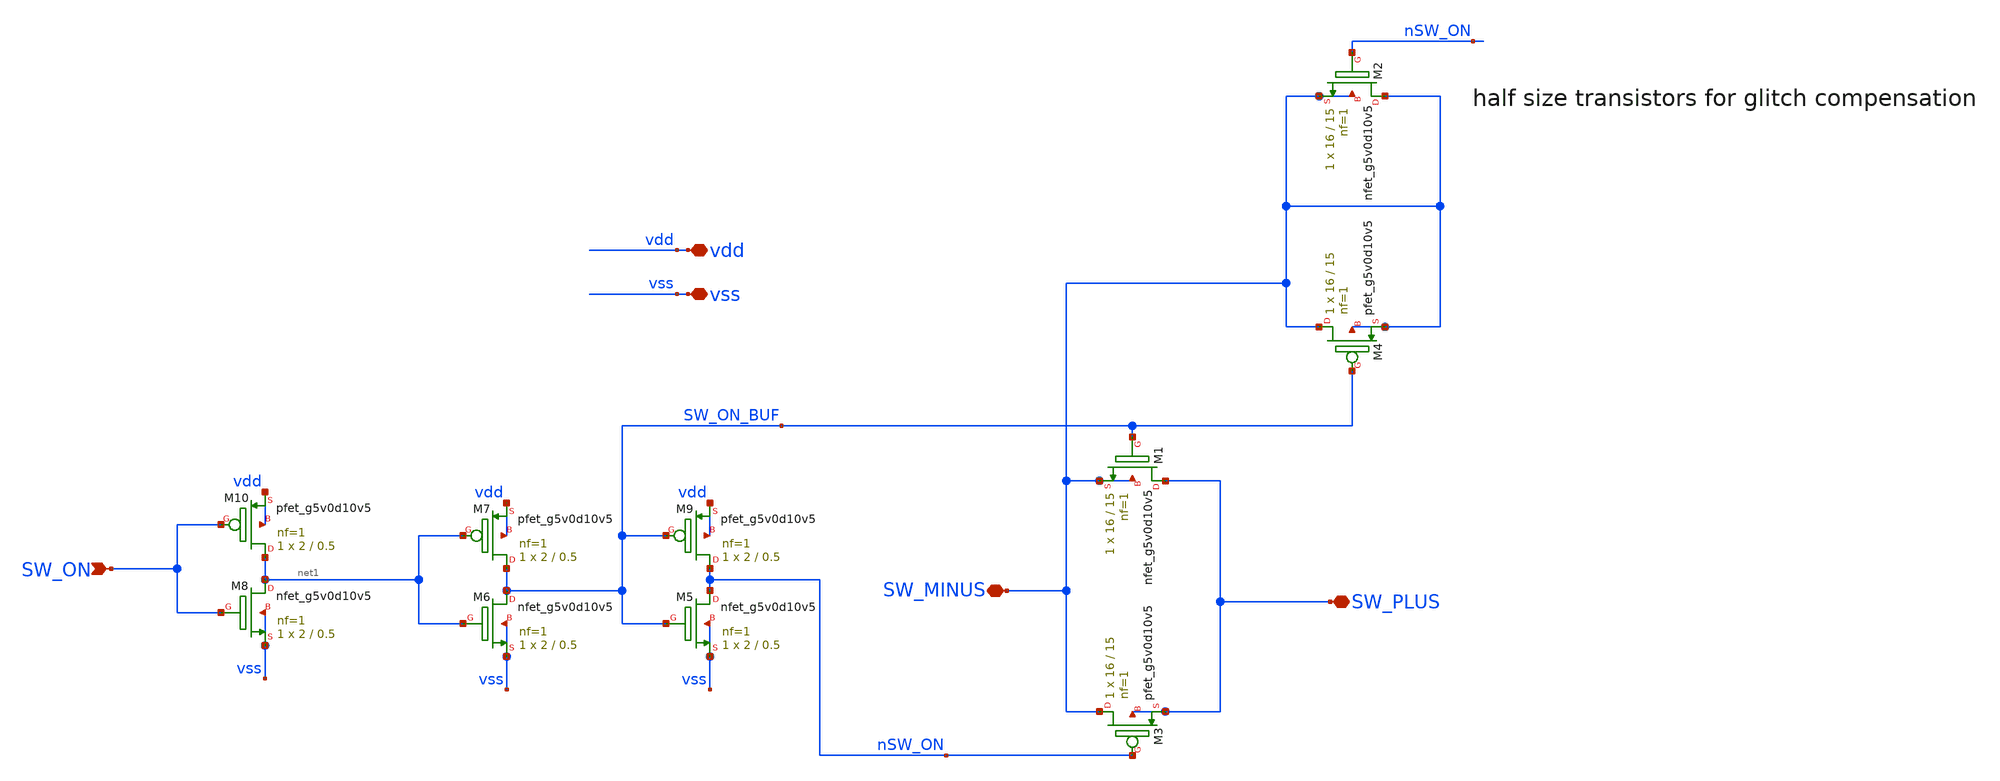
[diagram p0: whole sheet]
** sch_path: xschem/analog_switch.sch
**.subckt analog_switch vdd vss SW_ON SW_MINUS SW_PLUS
*.iopin vdd
*.iopin vss
*.ipin SW_ON
*.iopin SW_MINUS
*.iopin SW_PLUS
XM1 SW_PLUS SW_ON_BUF SW_MINUS SW_MINUS sky130_fd_pr__nfet_g5v0d10v5 L=15 W=16 nf=1 ad='int((1 + 1)/2) * 16 / 1 * 0.29'
+ as='int((1 + 2)/2) * 16 / 1 * 0.29' pd='2*int((1 + 1)/2) * (16 / 1 + 0.29)' ps='2*int((1 + 2)/2) * (16 / 1 + 0.29)'
+ nrd='0.29 / 16 ' nrs='0.29 / 16 ' sa=0 sb=0 sd=0 mult=1 m=1
XM3 SW_MINUS nSW_ON SW_PLUS SW_PLUS sky130_fd_pr__pfet_g5v0d10v5 L=15 W=16 nf=1 ad='int((1 + 1)/2) * 16 / 1 * 0.29'
+ as='int((1 + 2)/2) * 16 / 1 * 0.29' pd='2*int((1 + 1)/2) * (16 / 1 + 0.29)' ps='2*int((1 + 2)/2) * (16 / 1 + 0.29)'
+ nrd='0.29 / 16 ' nrs='0.29 / 16 ' sa=0 sb=0 sd=0 mult=1 m=1
XM2 SW_MINUS nSW_ON SW_MINUS SW_MINUS sky130_fd_pr__nfet_g5v0d10v5 L=15 W=16 nf=1 ad='int((1 + 1)/2) * 16 / 1 * 0.29'
+ as='int((1 + 2)/2) * 16 / 1 * 0.29' pd='2*int((1 + 1)/2) * (16 / 1 + 0.29)' ps='2*int((1 + 2)/2) * (16 / 1 + 0.29)'
+ nrd='0.29 / 16 ' nrs='0.29 / 16 ' sa=0 sb=0 sd=0 mult=1 m=1
XM4 SW_MINUS SW_ON_BUF SW_MINUS SW_MINUS sky130_fd_pr__pfet_g5v0d10v5 L=15 W=16 nf=1 ad='int((1 + 1)/2) * 16 / 1 * 0.29'
+ as='int((1 + 2)/2) * 16 / 1 * 0.29' pd='2*int((1 + 1)/2) * (16 / 1 + 0.29)' ps='2*int((1 + 2)/2) * (16 / 1 + 0.29)'
+ nrd='0.29 / 16 ' nrs='0.29 / 16 ' sa=0 sb=0 sd=0 mult=1 m=1
XM6 SW_ON_BUF net1 vss vss sky130_fd_pr__nfet_g5v0d10v5 L=0.5 W=2 nf=1 ad='int((1 + 1)/2) * 2 / 1 * 0.29'
+ as='int((1 + 2)/2) * 2 / 1 * 0.29' pd='2*int((1 + 1)/2) * (2 / 1 + 0.29)' ps='2*int((1 + 2)/2) * (2 / 1 + 0.29)'
+ nrd='0.29 / 2 ' nrs='0.29 / 2 ' sa=0 sb=0 sd=0 mult=1 m=1
XM7 SW_ON_BUF net1 vdd vdd sky130_fd_pr__pfet_g5v0d10v5 L=0.5 W=2 nf=1 ad='int((1 + 1)/2) * 2 / 1 * 0.29'
+ as='int((1 + 2)/2) * 2 / 1 * 0.29' pd='2*int((1 + 1)/2) * (2 / 1 + 0.29)' ps='2*int((1 + 2)/2) * (2 / 1 + 0.29)'
+ nrd='0.29 / 2 ' nrs='0.29 / 2 ' sa=0 sb=0 sd=0 mult=1 m=1
XM8 net1 SW_ON vss vss sky130_fd_pr__nfet_g5v0d10v5 L=0.5 W=2 nf=1 ad='int((1 + 1)/2) * 2 / 1 * 0.29'
+ as='int((1 + 2)/2) * 2 / 1 * 0.29' pd='2*int((1 + 1)/2) * (2 / 1 + 0.29)' ps='2*int((1 + 2)/2) * (2 / 1 + 0.29)'
+ nrd='0.29 / 2 ' nrs='0.29 / 2 ' sa=0 sb=0 sd=0 mult=1 m=1
XM10 net1 SW_ON vdd vdd sky130_fd_pr__pfet_g5v0d10v5 L=0.5 W=2 nf=1 ad='int((1 + 1)/2) * 2 / 1 * 0.29'
+ as='int((1 + 2)/2) * 2 / 1 * 0.29' pd='2*int((1 + 1)/2) * (2 / 1 + 0.29)' ps='2*int((1 + 2)/2) * (2 / 1 + 0.29)'
+ nrd='0.29 / 2 ' nrs='0.29 / 2 ' sa=0 sb=0 sd=0 mult=1 m=1
XM5 nSW_ON SW_ON_BUF vss vss sky130_fd_pr__nfet_g5v0d10v5 L=0.5 W=2 nf=1 ad='int((1 + 1)/2) * 2 / 1 * 0.29'
+ as='int((1 + 2)/2) * 2 / 1 * 0.29' pd='2*int((1 + 1)/2) * (2 / 1 + 0.29)' ps='2*int((1 + 2)/2) * (2 / 1 + 0.29)'
+ nrd='0.29 / 2 ' nrs='0.29 / 2 ' sa=0 sb=0 sd=0 mult=1 m=1
XM9 nSW_ON SW_ON_BUF vdd vdd sky130_fd_pr__pfet_g5v0d10v5 L=0.5 W=2 nf=1 ad='int((1 + 1)/2) * 2 / 1 * 0.29'
+ as='int((1 + 2)/2) * 2 / 1 * 0.29' pd='2*int((1 + 1)/2) * (2 / 1 + 0.29)' ps='2*int((1 + 2)/2) * (2 / 1 + 0.29)'
+ nrd='0.29 / 2 ' nrs='0.29 / 2 ' sa=0 sb=0 sd=0 mult=1 m=1
**.ends
.end
